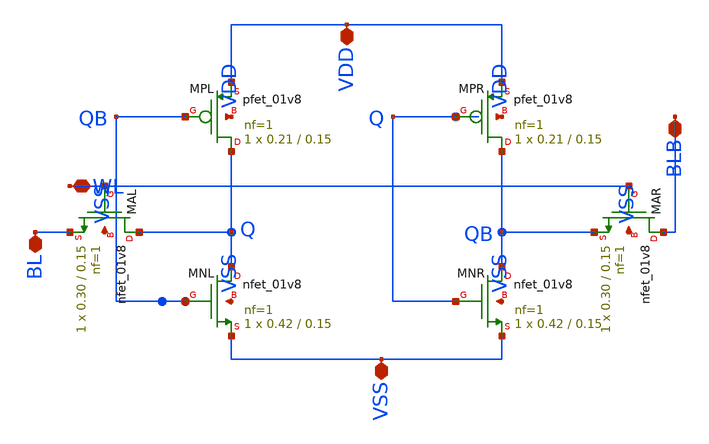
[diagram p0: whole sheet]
** sch_path: cells/bitcell_6t.sch
**.subckt bitcell_6t VDD BL BLB VSS WL
*.iopin VDD
*.iopin BL
*.iopin BLB
*.iopin VSS
*.iopin WL
XMPL Q QB VDD VDD sky130_fd_pr__pfet_01v8 L=0.15 W=0.21 nf=1 ad='W * 0.29' as='W * 0.29' pd='W + 2 * 0.29'
+ ps='W + 2 * 0.29' nrd=0 nrs=0 sa=0 sb=0 sd=0 mult=1 m=1
XMNL Q QB VSS VSS sky130_fd_pr__nfet_01v8 L=0.15 W=0.42 nf=1 ad='W * 0.29' as='W * 0.29' pd='W + 2 * 0.29'
+ ps='W + 2 * 0.29' nrd=0 nrs=0 sa=0 sb=0 sd=0 mult=1 m=1
XMPR QB Q VDD VDD sky130_fd_pr__pfet_01v8 L=0.15 W=0.21 nf=1 ad='W * 0.29' as='W * 0.29' pd='W + 2 * 0.29'
+ ps='W + 2 * 0.29' nrd=0 nrs=0 sa=0 sb=0 sd=0 mult=1 m=1
XMNR QB Q VSS VSS sky130_fd_pr__nfet_01v8 L=0.15 W=0.42 nf=1 ad='W * 0.29' as='W * 0.29' pd='W + 2 * 0.29'
+ ps='W + 2 * 0.29' nrd=0 nrs=0 sa=0 sb=0 sd=0 mult=1 m=1
XMAL Q WL BL VSS sky130_fd_pr__nfet_01v8 L=0.15 W=0.30 nf=1 ad='W * 0.29' as='W * 0.29' pd='W + 2 * 0.29'
+ ps='W + 2 * 0.29' nrd=0 nrs=0 sa=0 sb=0 sd=0 mult=1 m=1
XMAR BLB WL QB VSS sky130_fd_pr__nfet_01v8 L=0.15 W=0.30 nf=1 ad='W * 0.29' as='W * 0.29' pd='W + 2 * 0.29'
+ ps='W + 2 * 0.29' nrd=0 nrs=0 sa=0 sb=0 sd=0 mult=1 m=1
**.ends
.end
